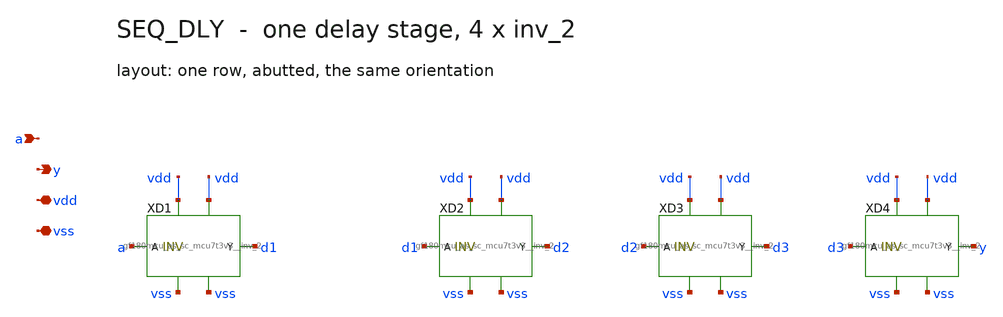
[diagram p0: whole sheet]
** sch_path: mixed_signal/sample_seq/seq_dly.sch
**.subckt seq_dly a y vdd vss
*.ipin a
*.opin y
*.iopin vdd
*.iopin vss
XD1 vdd vdd vss vss d1 a gf180mcu_as_sc_mcu7t3v3__inv_2
XD2 vdd vdd vss vss d2 d1 gf180mcu_as_sc_mcu7t3v3__inv_2
XD3 vdd vdd vss vss d3 d2 gf180mcu_as_sc_mcu7t3v3__inv_2
XD4 vdd vdd vss vss y d3 gf180mcu_as_sc_mcu7t3v3__inv_2
**.ends
.end
